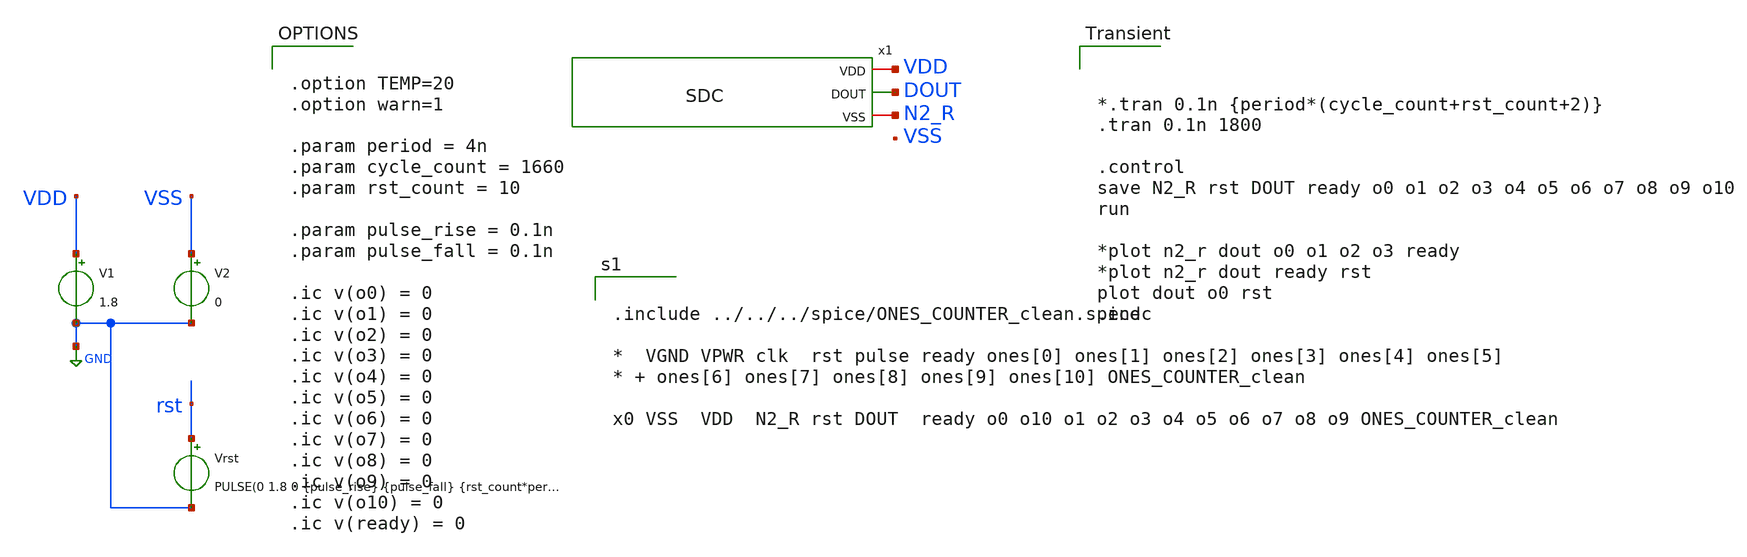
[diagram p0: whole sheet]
** sch_path: modules/ONES_COUNTER/test/dout_counter.sch
**.subckt dout_counter
V1 VDD GND 1.8
V2 VSS GND 0
Vrst rst GND PULSE(0 1.8 0 {pulse_rise} {pulse_fall} {rst_count*period} {rst_count*period} 1)
x1 VDD DOUT N2_R SDC
**** begin user architecture code



*.tran 0.1n {period*(cycle_count+rst_count+2)}
.tran 0.1n 1800

.control
save N2_R rst DOUT ready o0 o1 o2 o3 o4 o5 o6 o7 o8 o9 o10
run

*plot n2_r dout o0 o1 o2 o3 ready
*plot n2_r dout ready rst
plot dout o0 rst
.endc



.option TEMP=20
.option warn=1

.param period = 4n
.param cycle_count = 1660
.param rst_count = 10

.param pulse_rise = 0.1n
.param pulse_fall = 0.1n

.ic v(o0) = 0
.ic v(o1) = 0
.ic v(o2) = 0
.ic v(o3) = 0
.ic v(o4) = 0
.ic v(o5) = 0
.ic v(o6) = 0
.ic v(o7) = 0
.ic v(o8) = 0
.ic v(o9) = 0
.ic v(o10) = 0
.ic v(ready) = 0



.lib $env(PDK_ROOT)/$env(PDK)/libs.tech/combined/sky130.lib.spice tt
*.lib $env(PDK_ROOT)/$env(PDK)/libs.tech/ngspice/sky130.lib.spice tt

.include $env(PDK_ROOT)/$env(PDK)/libs.ref/sky130_fd_sc_hd/spice/sky130_fd_sc_hd.spice



.include ../../../spice/ONES_COUNTER_clean.spice

*  VGND VPWR clk  rst pulse ready ones[0] ones[1] ones[2] ones[3] ones[4] ones[5]
* + ones[6] ones[7] ones[8] ones[9] ones[10] ONES_COUNTER_clean

x0 VSS  VDD  N2_R rst DOUT  ready o0 o10 o1 o2 o3 o4 o5 o6 o7 o8 o9 ONES_COUNTER_clean


**** end user architecture code
**.ends
.GLOBAL GND
.end
